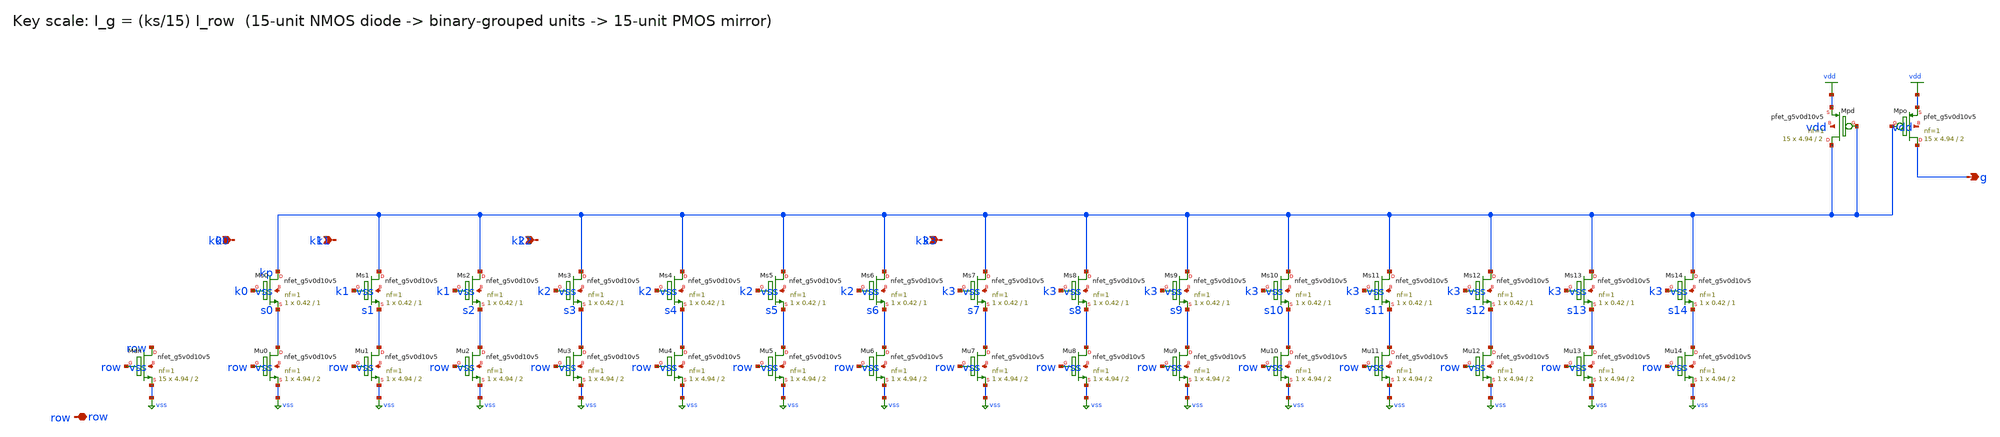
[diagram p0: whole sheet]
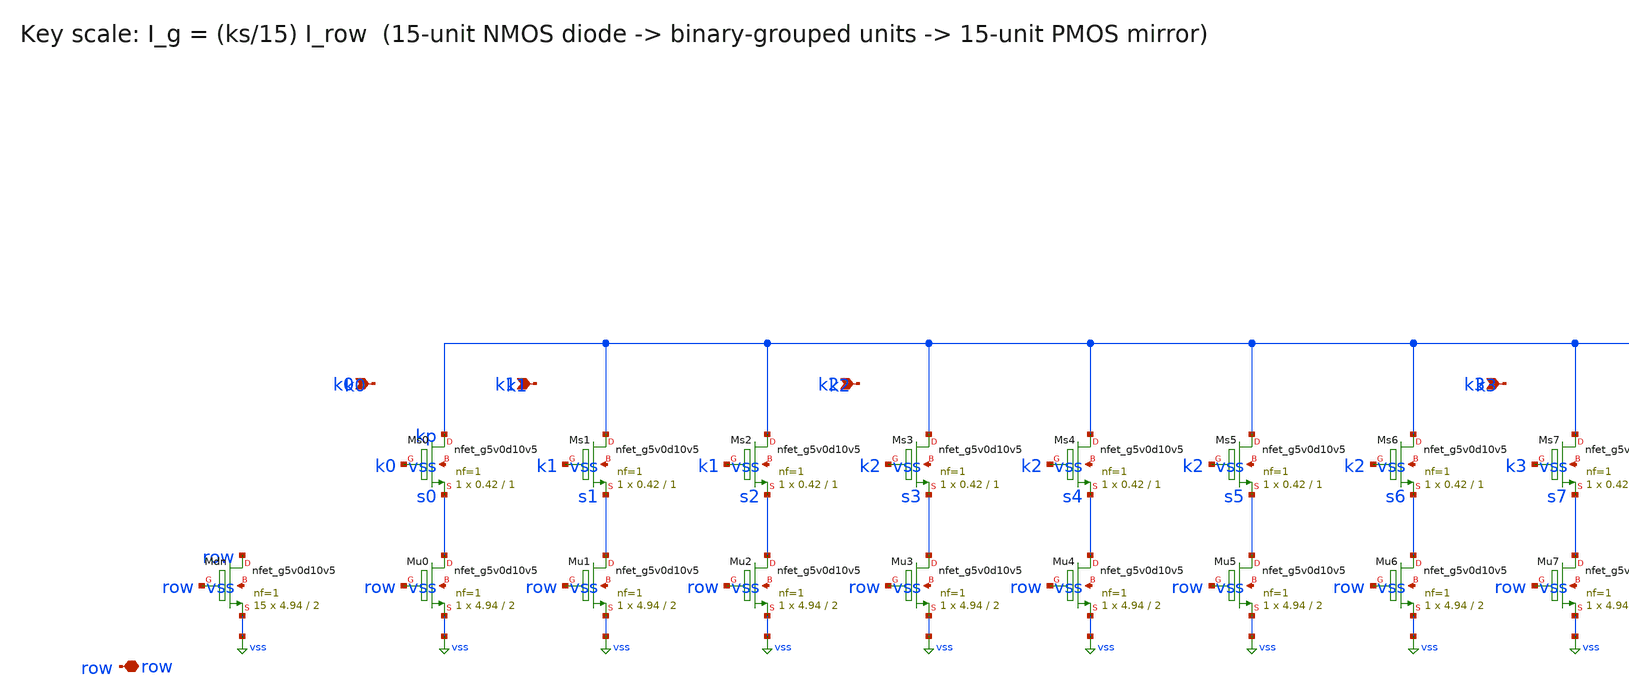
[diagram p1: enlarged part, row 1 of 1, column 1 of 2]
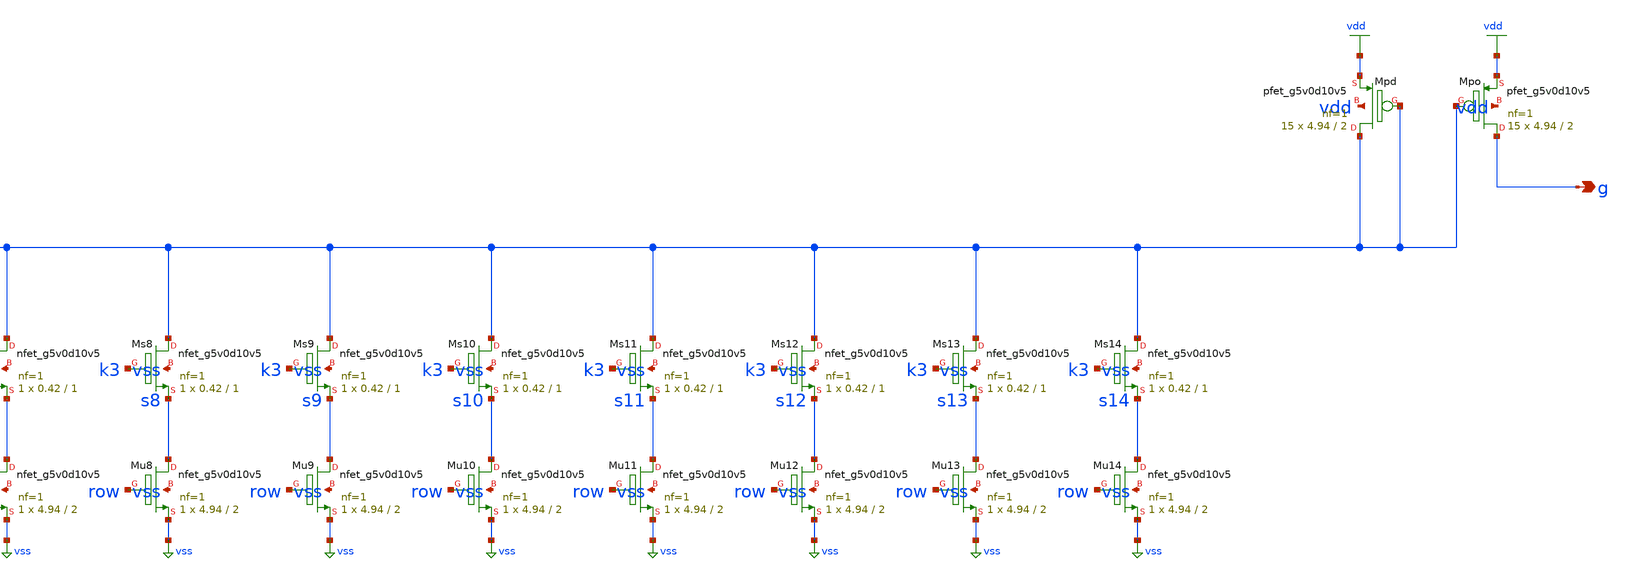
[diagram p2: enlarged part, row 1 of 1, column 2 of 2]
** sch_path: xschem/rt5w_kscale.sch
**.subckt rt5w_kscale k0 k1 k2 k3 row g
*.ipin k0
*.ipin k1
*.ipin k2
*.ipin k3
*.iopin row
*.opin g
XMdn row row vss vss sky130_fd_pr__nfet_g5v0d10v5 L=2 W=4.94 nf=1 ad=1.433 as=1.433 pd=10.46
+ ps=10.46 nrd=0.0587 nrs=0.0587 sa=0 sb=0 sd=0 mult=15 m=15
XMu0 s0 row vss vss sky130_fd_pr__nfet_g5v0d10v5 L=2 W=4.94 nf=1 ad=1.433 as=1.433 pd=10.46 ps=10.46
+ nrd=0.0587 nrs=0.0587 sa=0 sb=0 sd=0 mult=1 m=1
XMs0 kp k0 s0 vss sky130_fd_pr__nfet_g5v0d10v5 L=1 W=0.42 nf=1 ad=0.1218 as=0.1218 pd=1.42 ps=1.42
+ nrd=0.6905 nrs=0.6905 sa=0 sb=0 sd=0 mult=1 m=1
XMu1 s1 row vss vss sky130_fd_pr__nfet_g5v0d10v5 L=2 W=4.94 nf=1 ad=1.433 as=1.433 pd=10.46 ps=10.46
+ nrd=0.0587 nrs=0.0587 sa=0 sb=0 sd=0 mult=1 m=1
XMs1 kp k1 s1 vss sky130_fd_pr__nfet_g5v0d10v5 L=1 W=0.42 nf=1 ad=0.1218 as=0.1218 pd=1.42 ps=1.42
+ nrd=0.6905 nrs=0.6905 sa=0 sb=0 sd=0 mult=1 m=1
XMu2 s2 row vss vss sky130_fd_pr__nfet_g5v0d10v5 L=2 W=4.94 nf=1 ad=1.433 as=1.433 pd=10.46 ps=10.46
+ nrd=0.0587 nrs=0.0587 sa=0 sb=0 sd=0 mult=1 m=1
XMs2 kp k1 s2 vss sky130_fd_pr__nfet_g5v0d10v5 L=1 W=0.42 nf=1 ad=0.1218 as=0.1218 pd=1.42 ps=1.42
+ nrd=0.6905 nrs=0.6905 sa=0 sb=0 sd=0 mult=1 m=1
XMu3 s3 row vss vss sky130_fd_pr__nfet_g5v0d10v5 L=2 W=4.94 nf=1 ad=1.433 as=1.433 pd=10.46 ps=10.46
+ nrd=0.0587 nrs=0.0587 sa=0 sb=0 sd=0 mult=1 m=1
XMs3 kp k2 s3 vss sky130_fd_pr__nfet_g5v0d10v5 L=1 W=0.42 nf=1 ad=0.1218 as=0.1218 pd=1.42 ps=1.42
+ nrd=0.6905 nrs=0.6905 sa=0 sb=0 sd=0 mult=1 m=1
XMu4 s4 row vss vss sky130_fd_pr__nfet_g5v0d10v5 L=2 W=4.94 nf=1 ad=1.433 as=1.433 pd=10.46 ps=10.46
+ nrd=0.0587 nrs=0.0587 sa=0 sb=0 sd=0 mult=1 m=1
XMs4 kp k2 s4 vss sky130_fd_pr__nfet_g5v0d10v5 L=1 W=0.42 nf=1 ad=0.1218 as=0.1218 pd=1.42 ps=1.42
+ nrd=0.6905 nrs=0.6905 sa=0 sb=0 sd=0 mult=1 m=1
XMu5 s5 row vss vss sky130_fd_pr__nfet_g5v0d10v5 L=2 W=4.94 nf=1 ad=1.433 as=1.433 pd=10.46 ps=10.46
+ nrd=0.0587 nrs=0.0587 sa=0 sb=0 sd=0 mult=1 m=1
XMs5 kp k2 s5 vss sky130_fd_pr__nfet_g5v0d10v5 L=1 W=0.42 nf=1 ad=0.1218 as=0.1218 pd=1.42 ps=1.42
+ nrd=0.6905 nrs=0.6905 sa=0 sb=0 sd=0 mult=1 m=1
XMu6 s6 row vss vss sky130_fd_pr__nfet_g5v0d10v5 L=2 W=4.94 nf=1 ad=1.433 as=1.433 pd=10.46 ps=10.46
+ nrd=0.0587 nrs=0.0587 sa=0 sb=0 sd=0 mult=1 m=1
XMs6 kp k2 s6 vss sky130_fd_pr__nfet_g5v0d10v5 L=1 W=0.42 nf=1 ad=0.1218 as=0.1218 pd=1.42 ps=1.42
+ nrd=0.6905 nrs=0.6905 sa=0 sb=0 sd=0 mult=1 m=1
XMu7 s7 row vss vss sky130_fd_pr__nfet_g5v0d10v5 L=2 W=4.94 nf=1 ad=1.433 as=1.433 pd=10.46 ps=10.46
+ nrd=0.0587 nrs=0.0587 sa=0 sb=0 sd=0 mult=1 m=1
XMs7 kp k3 s7 vss sky130_fd_pr__nfet_g5v0d10v5 L=1 W=0.42 nf=1 ad=0.1218 as=0.1218 pd=1.42 ps=1.42
+ nrd=0.6905 nrs=0.6905 sa=0 sb=0 sd=0 mult=1 m=1
XMu8 s8 row vss vss sky130_fd_pr__nfet_g5v0d10v5 L=2 W=4.94 nf=1 ad=1.433 as=1.433 pd=10.46 ps=10.46
+ nrd=0.0587 nrs=0.0587 sa=0 sb=0 sd=0 mult=1 m=1
XMs8 kp k3 s8 vss sky130_fd_pr__nfet_g5v0d10v5 L=1 W=0.42 nf=1 ad=0.1218 as=0.1218 pd=1.42 ps=1.42
+ nrd=0.6905 nrs=0.6905 sa=0 sb=0 sd=0 mult=1 m=1
XMu9 s9 row vss vss sky130_fd_pr__nfet_g5v0d10v5 L=2 W=4.94 nf=1 ad=1.433 as=1.433 pd=10.46 ps=10.46
+ nrd=0.0587 nrs=0.0587 sa=0 sb=0 sd=0 mult=1 m=1
XMs9 kp k3 s9 vss sky130_fd_pr__nfet_g5v0d10v5 L=1 W=0.42 nf=1 ad=0.1218 as=0.1218 pd=1.42 ps=1.42
+ nrd=0.6905 nrs=0.6905 sa=0 sb=0 sd=0 mult=1 m=1
XMu10 s10 row vss vss sky130_fd_pr__nfet_g5v0d10v5 L=2 W=4.94 nf=1 ad=1.433 as=1.433 pd=10.46
+ ps=10.46 nrd=0.0587 nrs=0.0587 sa=0 sb=0 sd=0 mult=1 m=1
XMs10 kp k3 s10 vss sky130_fd_pr__nfet_g5v0d10v5 L=1 W=0.42 nf=1 ad=0.1218 as=0.1218 pd=1.42 ps=1.42
+ nrd=0.6905 nrs=0.6905 sa=0 sb=0 sd=0 mult=1 m=1
XMu11 s11 row vss vss sky130_fd_pr__nfet_g5v0d10v5 L=2 W=4.94 nf=1 ad=1.433 as=1.433 pd=10.46
+ ps=10.46 nrd=0.0587 nrs=0.0587 sa=0 sb=0 sd=0 mult=1 m=1
XMs11 kp k3 s11 vss sky130_fd_pr__nfet_g5v0d10v5 L=1 W=0.42 nf=1 ad=0.1218 as=0.1218 pd=1.42 ps=1.42
+ nrd=0.6905 nrs=0.6905 sa=0 sb=0 sd=0 mult=1 m=1
XMu12 s12 row vss vss sky130_fd_pr__nfet_g5v0d10v5 L=2 W=4.94 nf=1 ad=1.433 as=1.433 pd=10.46
+ ps=10.46 nrd=0.0587 nrs=0.0587 sa=0 sb=0 sd=0 mult=1 m=1
XMs12 kp k3 s12 vss sky130_fd_pr__nfet_g5v0d10v5 L=1 W=0.42 nf=1 ad=0.1218 as=0.1218 pd=1.42 ps=1.42
+ nrd=0.6905 nrs=0.6905 sa=0 sb=0 sd=0 mult=1 m=1
XMu13 s13 row vss vss sky130_fd_pr__nfet_g5v0d10v5 L=2 W=4.94 nf=1 ad=1.433 as=1.433 pd=10.46
+ ps=10.46 nrd=0.0587 nrs=0.0587 sa=0 sb=0 sd=0 mult=1 m=1
XMs13 kp k3 s13 vss sky130_fd_pr__nfet_g5v0d10v5 L=1 W=0.42 nf=1 ad=0.1218 as=0.1218 pd=1.42 ps=1.42
+ nrd=0.6905 nrs=0.6905 sa=0 sb=0 sd=0 mult=1 m=1
XMu14 s14 row vss vss sky130_fd_pr__nfet_g5v0d10v5 L=2 W=4.94 nf=1 ad=1.433 as=1.433 pd=10.46
+ ps=10.46 nrd=0.0587 nrs=0.0587 sa=0 sb=0 sd=0 mult=1 m=1
XMs14 kp k3 s14 vss sky130_fd_pr__nfet_g5v0d10v5 L=1 W=0.42 nf=1 ad=0.1218 as=0.1218 pd=1.42 ps=1.42
+ nrd=0.6905 nrs=0.6905 sa=0 sb=0 sd=0 mult=1 m=1
XMpd kp kp vdd vdd sky130_fd_pr__pfet_g5v0d10v5 L=2 W=4.94 nf=1 ad=1.433 as=1.433 pd=10.46 ps=10.46
+ nrd=0.0587 nrs=0.0587 sa=0 sb=0 sd=0 mult=15 m=15
XMpo g kp vdd vdd sky130_fd_pr__pfet_g5v0d10v5 L=2 W=4.94 nf=1 ad=1.433 as=1.433 pd=10.46 ps=10.46
+ nrd=0.0587 nrs=0.0587 sa=0 sb=0 sd=0 mult=15 m=15
**.ends
.GLOBAL vdd
.GLOBAL vss
.end
